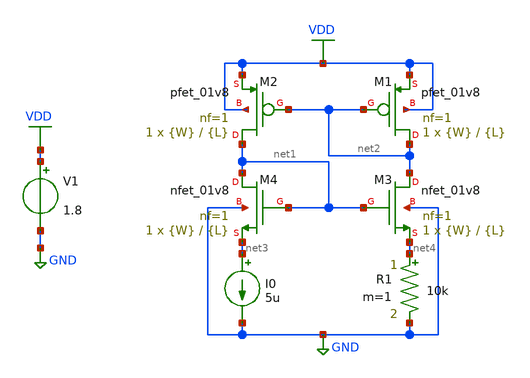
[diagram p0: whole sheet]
** sch_path: xschem/CMS.sch
**.subckt CMS
V1 VDD GND 1.8
XM1 net2 net2 VDD VDD sky130_fd_pr__pfet_01v8 L={L} W={W} nf=1 ad='int((nf+1)/2) * W/nf * 0.29' as='int((nf+2)/2) * W/nf * 0.29'
+ pd='2*int((nf+1)/2) * (W/nf + 0.29)' ps='2*int((nf+2)/2) * (W/nf + 0.29)' nrd='0.29 / W' nrs='0.29 / W'
+ sa=0 sb=0 sd=0 mult=1 m=1
XM2 net1 net2 VDD VDD sky130_fd_pr__pfet_01v8 L={L} W={W} nf=1 ad='int((nf+1)/2) * W/nf * 0.29' as='int((nf+2)/2) * W/nf * 0.29'
+ pd='2*int((nf+1)/2) * (W/nf + 0.29)' ps='2*int((nf+2)/2) * (W/nf + 0.29)' nrd='0.29 / W' nrs='0.29 / W'
+ sa=0 sb=0 sd=0 mult=1 m=1
XM3 net2 net1 net4 GND sky130_fd_pr__nfet_01v8 L={L} W={W} nf=1 ad='int((nf+1)/2) * W/nf * 0.29' as='int((nf+2)/2) * W/nf * 0.29'
+ pd='2*int((nf+1)/2) * (W/nf + 0.29)' ps='2*int((nf+2)/2) * (W/nf + 0.29)' nrd='0.29 / W' nrs='0.29 / W'
+ sa=0 sb=0 sd=0 mult=1 m=1
XM4 net1 net1 net3 GND sky130_fd_pr__nfet_01v8 L={L} W={W} nf=1 ad='int((nf+1)/2) * W/nf * 0.29' as='int((nf+2)/2) * W/nf * 0.29'
+ pd='2*int((nf+1)/2) * (W/nf + 0.29)' ps='2*int((nf+2)/2) * (W/nf + 0.29)' nrd='0.29 / W' nrs='0.29 / W'
+ sa=0 sb=0 sd=0 mult=1 m=1
I0 net3 GND 5u
R1 net4 GND 10k m=1
**** begin user architecture code

** opencircuitdesign pdks install
.lib $::SKYWATER_MODELS/sky130.lib.spice tt




** Analysis Requests **
** Outputs Requests **
.option wnflag=1
.option savecurrents
.control
op
save all
write CMS.raw
.endc




.param L=2.8
.param W=1


**** end user architecture code
**.ends
.GLOBAL VDD
.GLOBAL GND
.end
